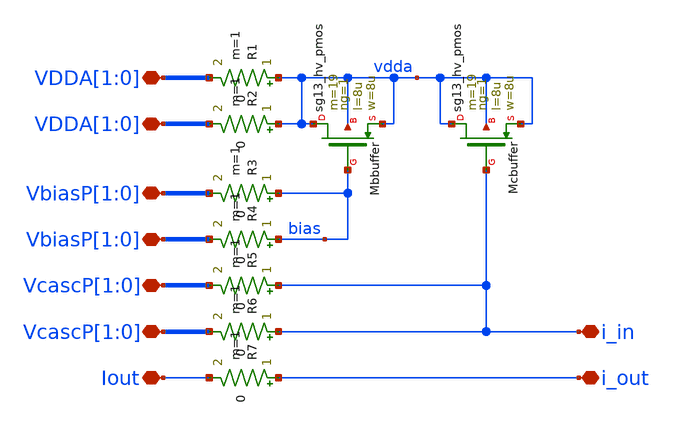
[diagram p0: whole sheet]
** sch_path: xschem/analog_wires.sch
**.subckt analog_wires VbiasP[1],VbiasP[0] VDDA[1],VDDA[0] VcascP[1],VcascP[0] Iout i_out i_in
*+ VDDA[1],VDDA[0] VbiasP[1],VbiasP[0] VcascP[1],VcascP[0]
*.iopin VbiasP[1],VbiasP[0]
*.iopin VDDA[1],VDDA[0]
*.iopin VcascP[1],VcascP[0]
*.iopin Iout
*.iopin i_out
*.iopin i_in
*.iopin VDDA[1],VDDA[0]
*.iopin VbiasP[1],VbiasP[0]
*.iopin VcascP[1],VcascP[0]
XMcbuffer vdda i_in vdda vdda sg13_hv_pmos w=8u l=8u ng=1 m=19 mm_ok=1
XMbbuffer vdda bias vdda vdda sg13_hv_pmos w=8u l=8u ng=1 m=19 mm_ok=1
R1 vdda VDDA[1] 0 m=1
R2 vdda VDDA[1] 0 m=1
R3 bias VbiasP[1] 0 m=1
R4 bias VbiasP[1] 0 m=1
R5 i_in VcascP[1] 0 m=1
R6 i_in VcascP[1] 0 m=1
R7 i_out Iout 0 m=1
**.ends
.end
